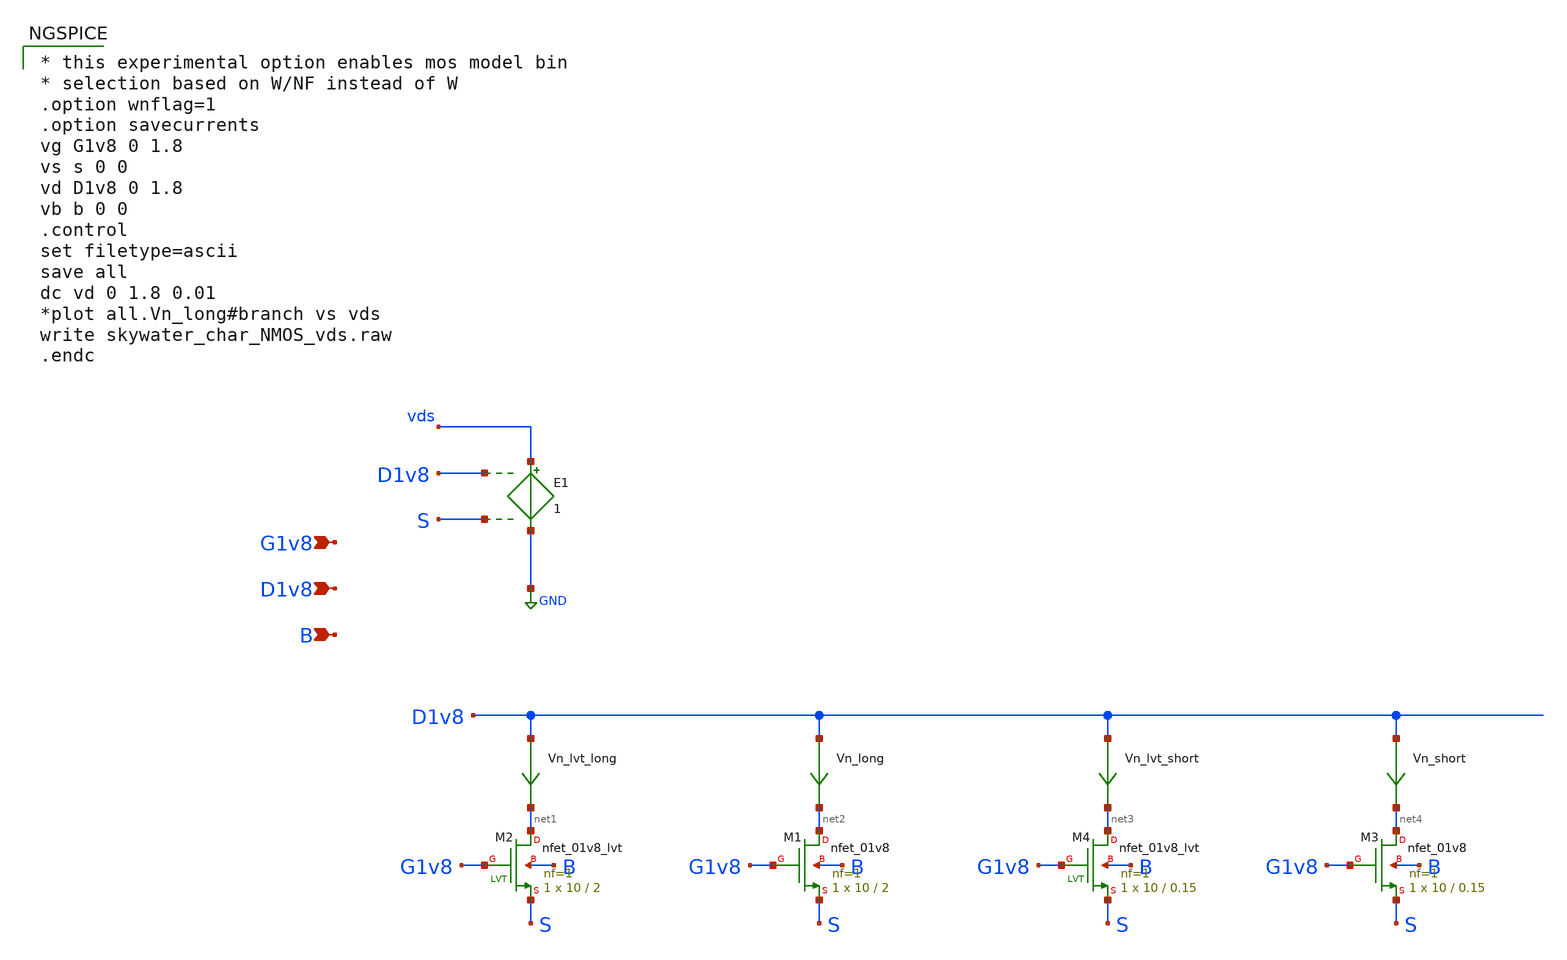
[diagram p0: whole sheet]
** sch_path: src/iCHIP/resources/char_schem_NMOS_vds.sch
* Copyright 2020 Stefan Frederik Schippers
* Licensed under the Apache License, Version 2.0 (the "License");
* you may not use this file except in compliance with the License.
* You may obtain a copy of the License at
* https://www.apache.org/licenses/LICENSE-2.0
* Unless required by applicable law or agreed to in writing, software
* distributed under the License is distributed on an "AS IS" BASIS,
* WITHOUT WARRANTIES OR CONDITIONS OF ANY KIND, either express or implied.
* See the License for the specific language governing permissions and
* limitations under the License.
**.subckt char_schem_NMOS_vds G1v8 D1v8 B
*.ipin G1v8
*.ipin D1v8
*.ipin B
Vn_lvt_long D1v8 net1 0
.save i(vn_lvt_long)
Vn_long D1v8 net2 0
.save i(vn_long)
Vn_lvt_short D1v8 net3 0
.save i(vn_lvt_short)
Vn_short D1v8 net4 0
.save i(vn_short)
XM1 net2 G1v8 S B sky130_fd_pr__nfet_01v8 L=2 W=10 nf=1 ad='int((nf+1)/2) * W/nf * 0.29' as='int((nf+2)/2) * W/nf * 0.29'
+ pd='2*int((nf+1)/2) * (W/nf + 0.29)' ps='2*int((nf+2)/2) * (W/nf + 0.29)' nrd='0.29 / W' nrs='0.29 / W'
+ sa=0 sb=0 sd=0 mult=1 m=1
XM2 net1 G1v8 S B sky130_fd_pr__nfet_01v8_lvt L=2 W=10 nf=1 ad='int((nf+1)/2) * W/nf * 0.29' as='int((nf+2)/2) * W/nf * 0.29'
+ pd='2*int((nf+1)/2) * (W/nf + 0.29)' ps='2*int((nf+2)/2) * (W/nf + 0.29)' nrd='0.29 / W' nrs='0.29 / W'
+ sa=0 sb=0 sd=0 mult=1 m=1
XM3 net4 G1v8 S B sky130_fd_pr__nfet_01v8 L=0.15 W=10 nf=1 ad='int((nf+1)/2) * W/nf * 0.29' as='int((nf+2)/2) * W/nf * 0.29'
+ pd='2*int((nf+1)/2) * (W/nf + 0.29)' ps='2*int((nf+2)/2) * (W/nf + 0.29)' nrd='0.29 / W' nrs='0.29 / W'
+ sa=0 sb=0 sd=0 mult=1 m=1
XM4 net3 G1v8 S B sky130_fd_pr__nfet_01v8_lvt L=0.15 W=10 nf=1 ad='int((nf+1)/2) * W/nf * 0.29' as='int((nf+2)/2) * W/nf * 0.29'
+ pd='2*int((nf+1)/2) * (W/nf + 0.29)' ps='2*int((nf+2)/2) * (W/nf + 0.29)' nrd='0.29 / W' nrs='0.29 / W'
+ sa=0 sb=0 sd=0 mult=1 m=1
E1 vds GND D1v8 S 1
**** begin user architecture code

.include $::SKYWATER_MODELS/cells/nfet_01v8/sky130_fd_pr__nfet_01v8__tt.corner.spice
.include $::SKYWATER_MODELS/cells/nfet_01v8_lvt/sky130_fd_pr__nfet_01v8_lvt__tt.corner.spice
.include $::SKYWATER_MODELS/cells/pfet_01v8/sky130_fd_pr__pfet_01v8__tt.corner.spice
.include $::SKYWATER_MODELS/cells/nfet_03v3_nvt/sky130_fd_pr__nfet_03v3_nvt__tt.corner.spice
.include $::SKYWATER_MODELS/cells/nfet_05v0_nvt/sky130_fd_pr__nfet_05v0_nvt__tt.corner.spice
.include $::SKYWATER_MODELS/cells/esd_nfet_01v8/sky130_fd_pr__esd_nfet_01v8__tt.corner.spice
.include $::SKYWATER_MODELS/cells/pfet_01v8_lvt/sky130_fd_pr__pfet_01v8_lvt__tt.corner.spice
.include $::SKYWATER_MODELS/cells/pfet_01v8_hvt/sky130_fd_pr__pfet_01v8_hvt__tt.corner.spice
.include $::SKYWATER_MODELS/cells/esd_pfet_g5v0d10v5/sky130_fd_pr__esd_pfet_g5v0d10v5__tt.corner.spice
.include $::SKYWATER_MODELS/cells/pfet_g5v0d10v5/sky130_fd_pr__pfet_g5v0d10v5__tt.corner.spice
.include $::SKYWATER_MODELS/cells/pfet_g5v0d16v0/sky130_fd_pr__pfet_g5v0d16v0__tt.corner.spice
.include $::SKYWATER_MODELS/cells/nfet_g5v0d10v5/sky130_fd_pr__nfet_g5v0d10v5__tt.corner.spice
.include $::SKYWATER_MODELS/cells/nfet_g5v0d16v0/sky130_fd_pr__nfet_g5v0d16v0__tt_discrete.corner.spice
.include $::SKYWATER_MODELS/cells/esd_nfet_g5v0d10v5/sky130_fd_pr__esd_nfet_g5v0d10v5__tt.corner.spice
.include $::SKYWATER_MODELS/models/corners/tt/nonfet.spice
* Mismatch parameters
.include $::SKYWATER_MODELS/cells/nfet_01v8/sky130_fd_pr__nfet_01v8__mismatch.corner.spice
.include $::SKYWATER_MODELS/cells/pfet_01v8/sky130_fd_pr__pfet_01v8__mismatch.corner.spice
.include $::SKYWATER_MODELS/cells/nfet_01v8_lvt/sky130_fd_pr__nfet_01v8_lvt__mismatch.corner.spice
.include $::SKYWATER_MODELS/cells/pfet_01v8_lvt/sky130_fd_pr__pfet_01v8_lvt__mismatch.corner.spice
.include $::SKYWATER_MODELS/cells/pfet_01v8_hvt/sky130_fd_pr__pfet_01v8_hvt__mismatch.corner.spice
.include $::SKYWATER_MODELS/cells/nfet_g5v0d10v5/sky130_fd_pr__nfet_g5v0d10v5__mismatch.corner.spice
.include $::SKYWATER_MODELS/cells/pfet_g5v0d10v5/sky130_fd_pr__pfet_g5v0d10v5__mismatch.corner.spice
.include $::SKYWATER_MODELS/cells/nfet_05v0_nvt/sky130_fd_pr__nfet_05v0_nvt__mismatch.corner.spice
.include $::SKYWATER_MODELS/cells/nfet_03v3_nvt/sky130_fd_pr__nfet_03v3_nvt__mismatch.corner.spice
* Resistor$::SKYWATER_MODELS/Capacitor
.include $::SKYWATER_MODELS/models/r+c/res_typical__cap_typical.spice
.include $::SKYWATER_MODELS/models/r+c/res_typical__cap_typical__lin.spice
* Special cells
.include $::SKYWATER_MODELS/models/corners/tt/specialized_cells.spice
* All models
.include $::SKYWATER_MODELS/models/all.spice
* Corner
.include $::SKYWATER_MODELS/models/corners/tt/rf.spice


* this experimental option enables mos model bin
* selection based on W/NF instead of W
.option wnflag=1
.option savecurrents
vg G1v8 0 1.8
vs s 0 0
vd D1v8 0 1.8
vb b 0 0
.control
set filetype=ascii
save all
dc vd 0 1.8 0.01
*plot all.Vn_long#branch vs vds
write skywater_char_NMOS_vds.raw
.endc



.include $::SKYWATER_MODELS/cells/nfet_20v0/sky130_fd_pr__nfet_20v0__tt_discrete.corner.spice

**** end user architecture code
**.ends
.GLOBAL GND
.end
